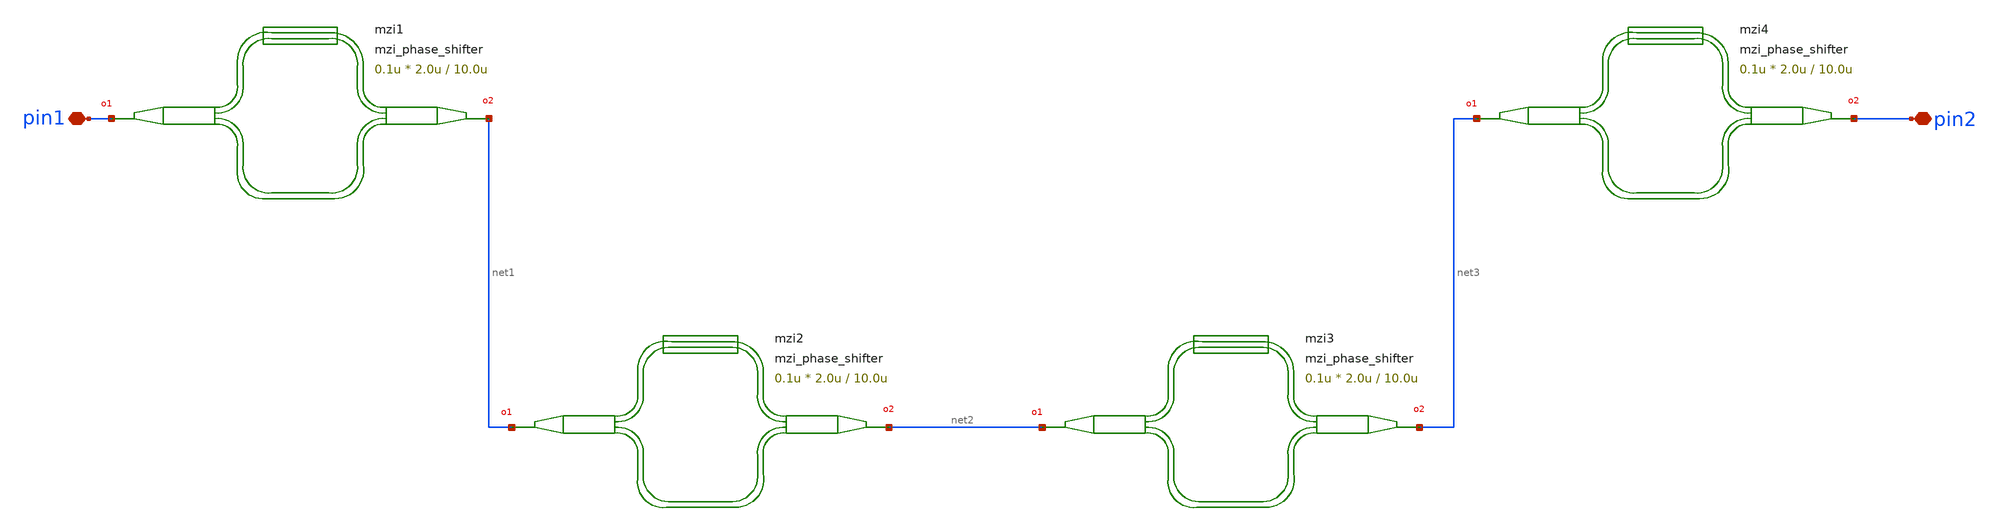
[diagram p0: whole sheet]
** sch_path: xschem/tests/test_sch/test_mzi_phase_shifter.sch
* Copyright (c) 2024, Mabrains LLC
* Licensed under the GNU Lesser General Public License, Version 3.0 (the "License");
* you may not use this file except in compliance with the License.
* GNU Lesser General Public License
* Version 3, 29 June 2007
* This program is free software: you can redistribute it and/or modify
* it under the terms of the GNU Lesser General Public License as published
* by the Free Software Foundation, either version 3 of the License, or
* (at your option) any later version.
* This program is distributed in the hope that it will be useful,
* but WITHOUT ANY WARRANTY; without even the implied warranty of
* MERCHANTABILITY or FITNESS FOR A PARTICULAR PURPOSE.  See the
* GNU Lesser General Public License for more details.
* You should have received a copy of the GNU Lesser General Public License
* along with this program.  If not, see <https://www.gnu.org/licenses/>.
* SPDX-License-Identifier: LGPL-3.0
**.subckt test_mzi_phase_shifter pin1 pin2
*.iopin pin1
*.iopin pin2
Pmzi2 net1 net2 mzi_phase_shifter delta_length=10.0u length_y=2.0u length_x=0.1u
Pmzi1 pin1 net1 mzi_phase_shifter delta_length=10.0u length_y=2.0u length_x=0.1u
Pmzi3 net2 net3 mzi_phase_shifter delta_length=10.0u length_y=2.0u length_x=0.1u
Pmzi4 net3 pin2 mzi_phase_shifter delta_length=10.0u length_y=2.0u length_x=0.1u
**.ends
.end
